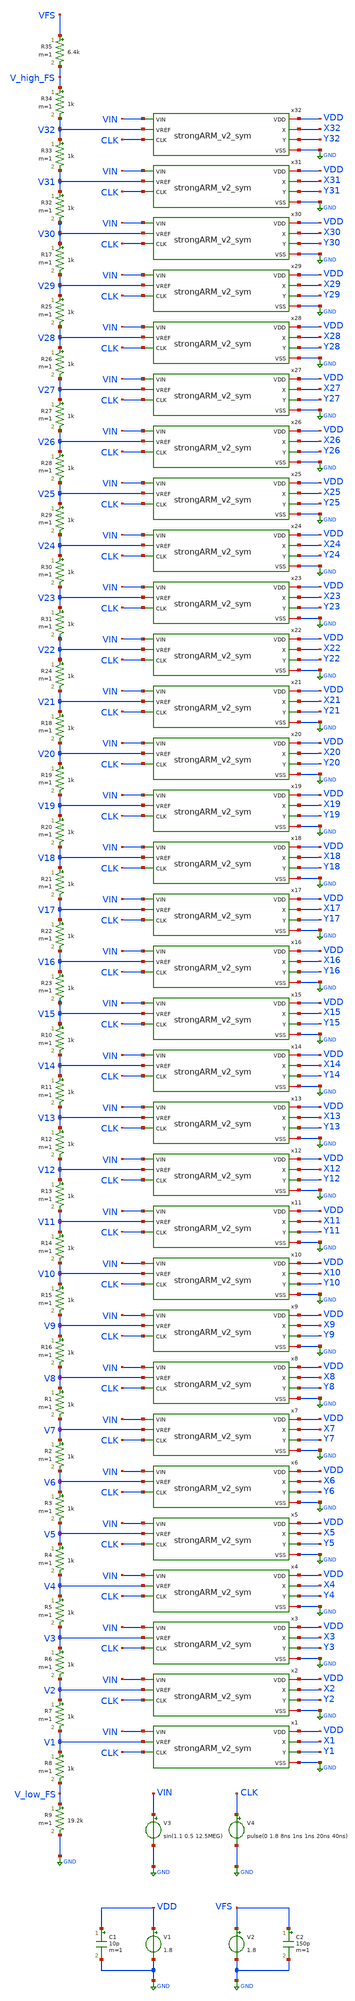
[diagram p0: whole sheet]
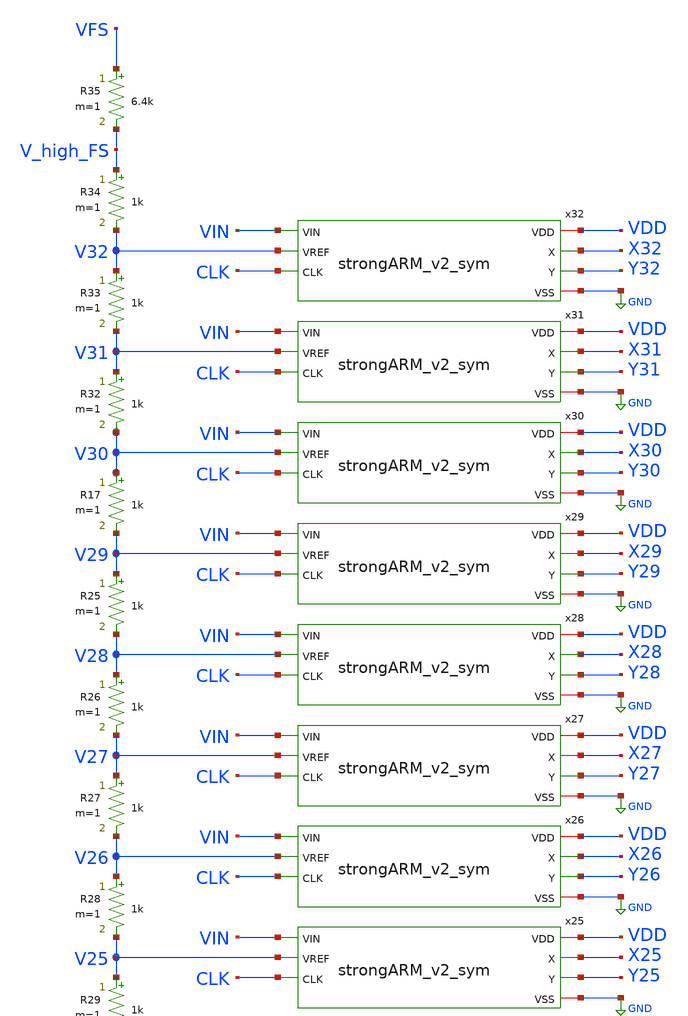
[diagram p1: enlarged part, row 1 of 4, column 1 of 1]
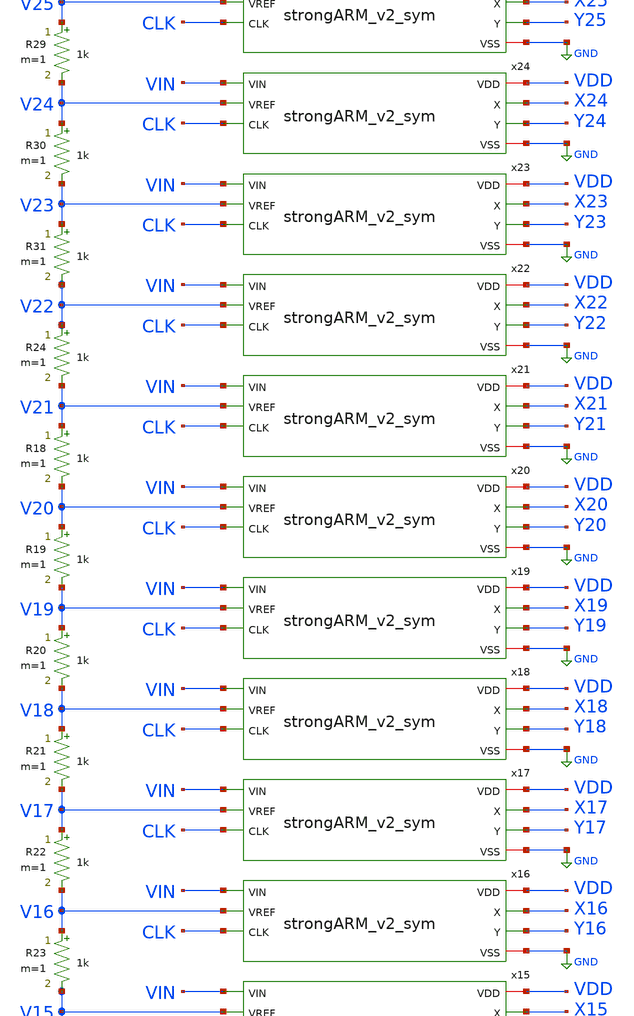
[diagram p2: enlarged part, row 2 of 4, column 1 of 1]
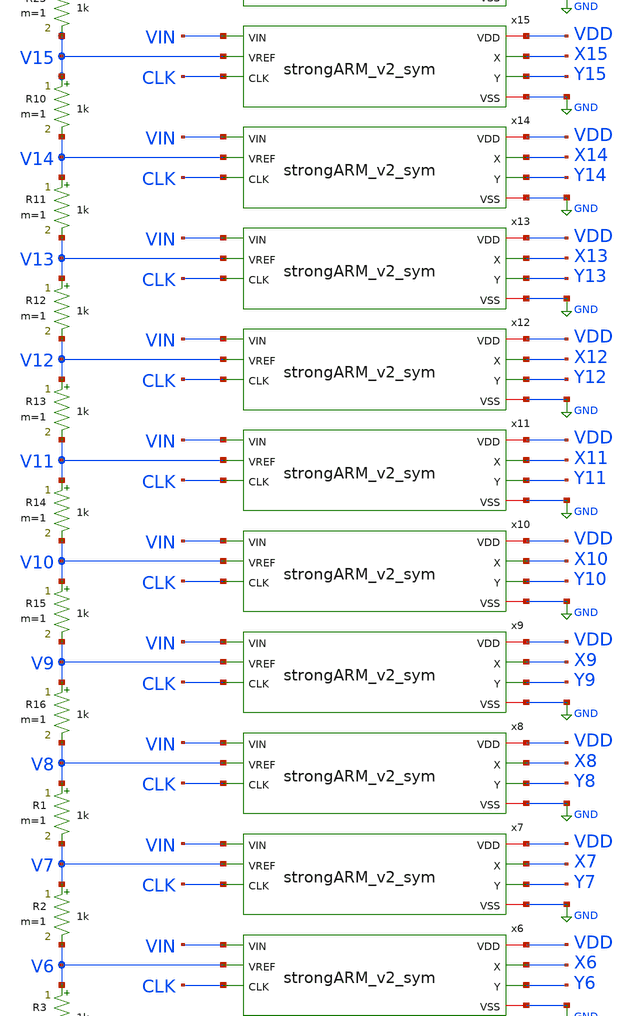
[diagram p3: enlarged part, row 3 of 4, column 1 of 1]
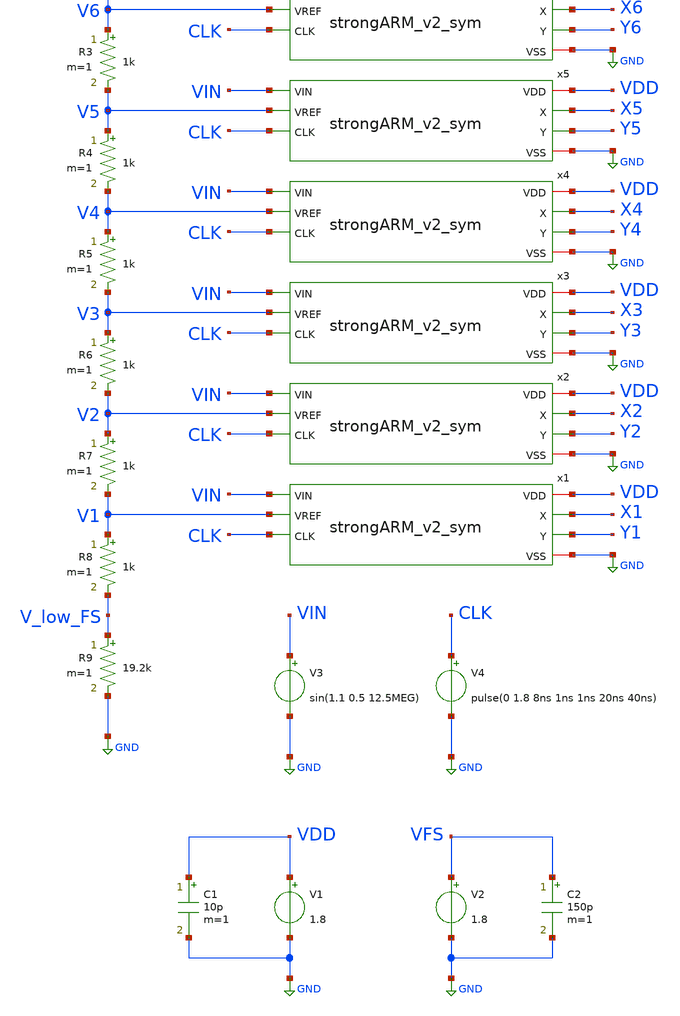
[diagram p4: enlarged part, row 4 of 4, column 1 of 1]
** sch_path: strongARM/flash_ADC_5b_v2.sch
**.subckt flash_ADC_5b_v2
R1 V8 V7 1k m=1
R2 V7 V6 1k m=1
R3 V6 V5 1k m=1
R4 V5 V4 1k m=1
R5 V4 V3 1k m=1
R6 V3 V2 1k m=1
R7 V2 V1 1k m=1
R8 V1 V_low_FS 1k m=1
R9 V_low_FS GND 19.2k m=1
R10 V15 V14 1k m=1
R11 V14 V13 1k m=1
R12 V13 V12 1k m=1
R13 V12 V11 1k m=1
R14 V11 V10 1k m=1
R15 V10 V9 1k m=1
R16 V9 V8 1k m=1
R18 V21 V20 1k m=1
R19 V20 V19 1k m=1
R20 V19 V18 1k m=1
R21 V18 V17 1k m=1
R22 V17 V16 1k m=1
R23 V16 V15 1k m=1
R24 V22 V21 1k m=1
R25 V29 V28 1k m=1
R26 V28 V27 1k m=1
R27 V27 V26 1k m=1
R28 V26 V25 1k m=1
R29 V25 V24 1k m=1
R30 V24 V23 1k m=1
R31 V23 V22 1k m=1
R17 V30 V29 1k m=1
R32 V31 V30 1k m=1
R33 V32 V31 1k m=1
R34 V_high_FS V32 1k m=1
R35 VFS V_high_FS 6.4k m=1
x1 VDD X1 Y1 VIN V1 CLK GND strongARM_v2_sym
x2 VDD X2 Y2 VIN V2 CLK GND strongARM_v2_sym
x3 VDD X3 Y3 VIN V3 CLK GND strongARM_v2_sym
x4 VDD X4 Y4 VIN V4 CLK GND strongARM_v2_sym
x5 VDD X5 Y5 VIN V5 CLK GND strongARM_v2_sym
x6 VDD X6 Y6 VIN V6 CLK GND strongARM_v2_sym
x7 VDD X7 Y7 VIN V7 CLK GND strongARM_v2_sym
x8 VDD X8 Y8 VIN V8 CLK GND strongARM_v2_sym
x9 VDD X9 Y9 VIN V9 CLK GND strongARM_v2_sym
x10 VDD X10 Y10 VIN V10 CLK GND strongARM_v2_sym
x11 VDD X11 Y11 VIN V11 CLK GND strongARM_v2_sym
x12 VDD X12 Y12 VIN V12 CLK GND strongARM_v2_sym
x13 VDD X13 Y13 VIN V13 CLK GND strongARM_v2_sym
x14 VDD X14 Y14 VIN V14 CLK GND strongARM_v2_sym
x15 VDD X15 Y15 VIN V15 CLK GND strongARM_v2_sym
x16 VDD X16 Y16 VIN V16 CLK GND strongARM_v2_sym
x17 VDD X17 Y17 VIN V17 CLK GND strongARM_v2_sym
x18 VDD X18 Y18 VIN V18 CLK GND strongARM_v2_sym
x19 VDD X19 Y19 VIN V19 CLK GND strongARM_v2_sym
x20 VDD X20 Y20 VIN V20 CLK GND strongARM_v2_sym
x21 VDD X21 Y21 VIN V21 CLK GND strongARM_v2_sym
x22 VDD X22 Y22 VIN V22 CLK GND strongARM_v2_sym
x23 VDD X23 Y23 VIN V23 CLK GND strongARM_v2_sym
x24 VDD X24 Y24 VIN V24 CLK GND strongARM_v2_sym
x25 VDD X25 Y25 VIN V25 CLK GND strongARM_v2_sym
x26 VDD X26 Y26 VIN V26 CLK GND strongARM_v2_sym
x27 VDD X27 Y27 VIN V27 CLK GND strongARM_v2_sym
x28 VDD X28 Y28 VIN V28 CLK GND strongARM_v2_sym
x29 VDD X29 Y29 VIN V29 CLK GND strongARM_v2_sym
x30 VDD X30 Y30 VIN V30 CLK GND strongARM_v2_sym
x31 VDD X31 Y31 VIN V31 CLK GND strongARM_v2_sym
x32 VDD X32 Y32 VIN V32 CLK GND strongARM_v2_sym
V3 VIN GND sin(1.1 0.5 12.5MEG)
V4 CLK GND pulse(0 1.8 8ns 1ns 1ns 20ns 40ns)
V1 VDD GND 1.8
V2 VFS GND 1.8
C1 VDD GND 10p m=1
C2 VFS GND 150p m=1
**** begin user architecture code
.lib $::SKYWATER_MODELS/sky130.lib.spice tt


.options savecurrents
.control

save all

tran 0.005n 120n
remzerovec
write flash_ADC_5b_v2.raw

.endc


**** end user architecture code
**.ends

* expanding   symbol:  /foss/designs/Analog_FA23_SP24/strongARM/strongARM_v2_sym.sym # of pins=7
** sym_path: strongARM/strongARM_v2_sym.sym
** sch_path: strongARM/strongARM_v2_sym.sch
.subckt strongARM_v2_sym VDD X Y VIN VREF CLK VSS
*.iopin VDD
*.ipin VIN
*.ipin VREF
*.opin Y
*.opin X
*.iopin VSS
*.ipin CLK
XM4 net2 CLK VDD VDD sky130_fd_pr__pfet_01v8_lvt L=0.35 W=1 nf=1 ad='int((nf+1)/2) * W/nf * 0.29' as='int((nf+2)/2) * W/nf * 0.29'
+ pd='2*int((nf+1)/2) * (W/nf + 0.29)' ps='2*int((nf+2)/2) * (W/nf + 0.29)' nrd='0.29 / W' nrs='0.29 / W'
+ sa=0 sb=0 sd=0 mult=1 m=1
XM1 X CLK VDD VDD sky130_fd_pr__pfet_01v8_lvt L=0.35 W=1 nf=1 ad='int((nf+1)/2) * W/nf * 0.29' as='int((nf+2)/2) * W/nf * 0.29'
+ pd='2*int((nf+1)/2) * (W/nf + 0.29)' ps='2*int((nf+2)/2) * (W/nf + 0.29)' nrd='0.29 / W' nrs='0.29 / W'
+ sa=0 sb=0 sd=0 mult=1 m=1
XM2 Y X VDD VDD sky130_fd_pr__pfet_01v8_lvt L=0.35 W=1 nf=1 ad='int((nf+1)/2) * W/nf * 0.29' as='int((nf+2)/2) * W/nf * 0.29'
+ pd='2*int((nf+1)/2) * (W/nf + 0.29)' ps='2*int((nf+2)/2) * (W/nf + 0.29)' nrd='0.29 / W' nrs='0.29 / W'
+ sa=0 sb=0 sd=0 mult=1 m=1
XM3 X Y VDD VDD sky130_fd_pr__pfet_01v8_lvt L=0.35 W=1 nf=1 ad='int((nf+1)/2) * W/nf * 0.29' as='int((nf+2)/2) * W/nf * 0.29'
+ pd='2*int((nf+1)/2) * (W/nf + 0.29)' ps='2*int((nf+2)/2) * (W/nf + 0.29)' nrd='0.29 / W' nrs='0.29 / W'
+ sa=0 sb=0 sd=0 mult=1 m=1
XM5 Y CLK VDD VDD sky130_fd_pr__pfet_01v8_lvt L=0.35 W=1 nf=1 ad='int((nf+1)/2) * W/nf * 0.29' as='int((nf+2)/2) * W/nf * 0.29'
+ pd='2*int((nf+1)/2) * (W/nf + 0.29)' ps='2*int((nf+2)/2) * (W/nf + 0.29)' nrd='0.29 / W' nrs='0.29 / W'
+ sa=0 sb=0 sd=0 mult=1 m=1
XM6 net3 CLK VDD VDD sky130_fd_pr__pfet_01v8_lvt L=0.35 W=1 nf=1 ad='int((nf+1)/2) * W/nf * 0.29' as='int((nf+2)/2) * W/nf * 0.29'
+ pd='2*int((nf+1)/2) * (W/nf + 0.29)' ps='2*int((nf+2)/2) * (W/nf + 0.29)' nrd='0.29 / W' nrs='0.29 / W'
+ sa=0 sb=0 sd=0 mult=1 m=1
XM10 X Y net2 VSS sky130_fd_pr__nfet_01v8_lvt L=0.15 W=1 nf=1 ad='int((nf+1)/2) * W/nf * 0.29' as='int((nf+2)/2) * W/nf * 0.29'
+ pd='2*int((nf+1)/2) * (W/nf + 0.29)' ps='2*int((nf+2)/2) * (W/nf + 0.29)' nrd='0.29 / W' nrs='0.29 / W'
+ sa=0 sb=0 sd=0 mult=1 m=1
XM7 Y X net3 VSS sky130_fd_pr__nfet_01v8_lvt L=0.15 W=1 nf=1 ad='int((nf+1)/2) * W/nf * 0.29' as='int((nf+2)/2) * W/nf * 0.29'
+ pd='2*int((nf+1)/2) * (W/nf + 0.29)' ps='2*int((nf+2)/2) * (W/nf + 0.29)' nrd='0.29 / W' nrs='0.29 / W'
+ sa=0 sb=0 sd=0 mult=1 m=1
XM8 net2 VIN net1 VSS sky130_fd_pr__nfet_01v8_lvt L=0.15 W=4 nf=1 ad='int((nf+1)/2) * W/nf * 0.29' as='int((nf+2)/2) * W/nf * 0.29'
+ pd='2*int((nf+1)/2) * (W/nf + 0.29)' ps='2*int((nf+2)/2) * (W/nf + 0.29)' nrd='0.29 / W' nrs='0.29 / W'
+ sa=0 sb=0 sd=0 mult=6 m=6
XM9 net3 VREF net1 VSS sky130_fd_pr__nfet_01v8_lvt L=0.15 W=4 nf=1 ad='int((nf+1)/2) * W/nf * 0.29' as='int((nf+2)/2) * W/nf * 0.29'
+ pd='2*int((nf+1)/2) * (W/nf + 0.29)' ps='2*int((nf+2)/2) * (W/nf + 0.29)' nrd='0.29 / W' nrs='0.29 / W'
+ sa=0 sb=0 sd=0 mult=6 m=6
XM11 net1 CLK VSS VSS sky130_fd_pr__nfet_01v8_lvt L=0.15 W=4 nf=1 ad='int((nf+1)/2) * W/nf * 0.29' as='int((nf+2)/2) * W/nf * 0.29'
+ pd='2*int((nf+1)/2) * (W/nf + 0.29)' ps='2*int((nf+2)/2) * (W/nf + 0.29)' nrd='0.29 / W' nrs='0.29 / W'
+ sa=0 sb=0 sd=0 mult=12 m=12
.ends

.GLOBAL GND
.end
